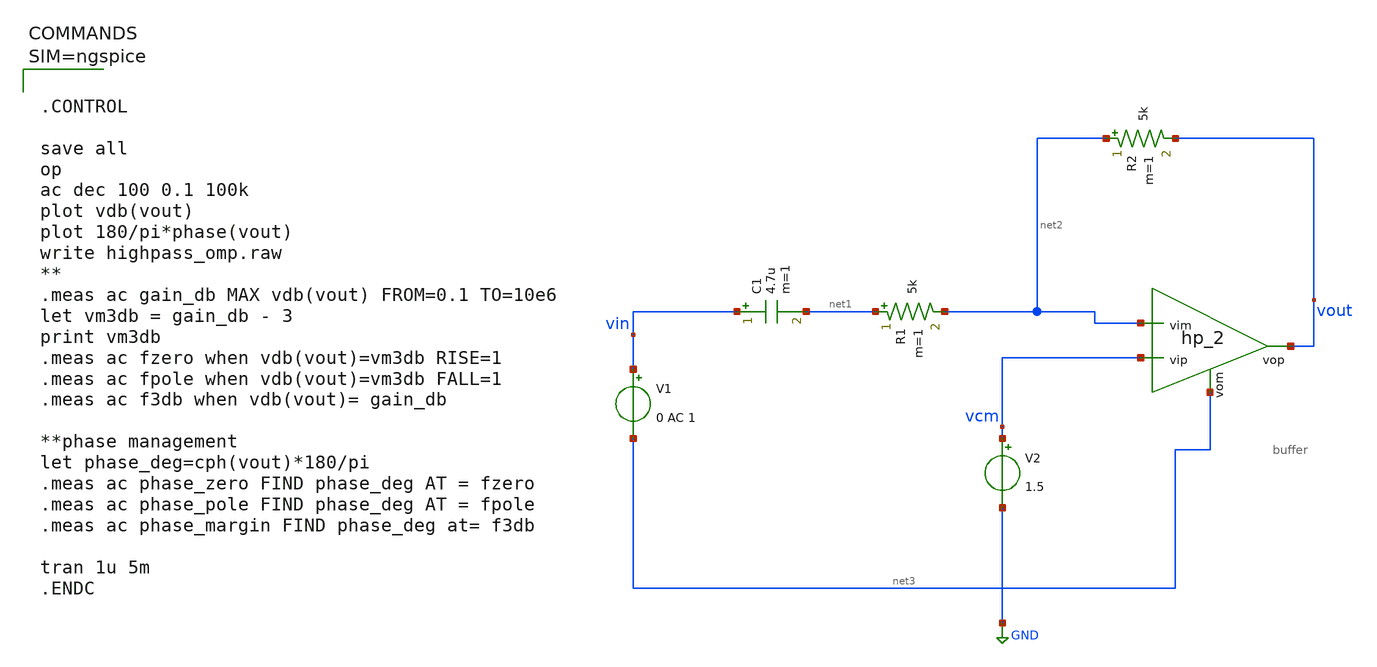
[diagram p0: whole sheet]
** sch_path: work/xschem/highpass_omp_2.sch
**.subckt highpass_omp_2
C1 vin net1 4.7u m=1
R1 net1 net2 5k m=1
V1 vin net3 0 AC 1
V2 vcm GND 1.5
R2 net2 vout 5k m=1
x1 vout vcm net2 net3 buffer
**** begin user architecture code



.CONTROL

save all
op
ac dec 100 0.1 100k
plot vdb(vout)
plot 180/pi*phase(vout)
write highpass_omp.raw
**
.meas ac gain_db MAX vdb(vout) FROM=0.1 TO=10e6
let vm3db = gain_db - 3
print vm3db
.meas ac fzero when vdb(vout)=vm3db RISE=1
.meas ac fpole when vdb(vout)=vm3db FALL=1
.meas ac f3db when vdb(vout)= gain_db

**phase management
let phase_deg=cph(vout)*180/pi
.meas ac phase_zero FIND phase_deg AT = fzero
.meas ac phase_pole FIND phase_deg AT = fpole
.meas ac phase_margin FIND phase_deg at= f3db

tran 1u 5m
.ENDC



**** end user architecture code
**.ends

* expanding   symbol:  buffer.sym # of pins=4
** sym_path: work/xschem/buffer.sym
** sch_path: work/xschem/buffer.sch
.subckt buffer vop vip vim vom
*.ipin vop
*.ipin vom
*.ipin vim
*.ipin vip
E1 net1 GND vip vim 1000
R1 net1 net2 200 m=1
C1 net2 GND 1u m=1
E2 vop vom net2 GND 1
.ends

.GLOBAL GND
.end
